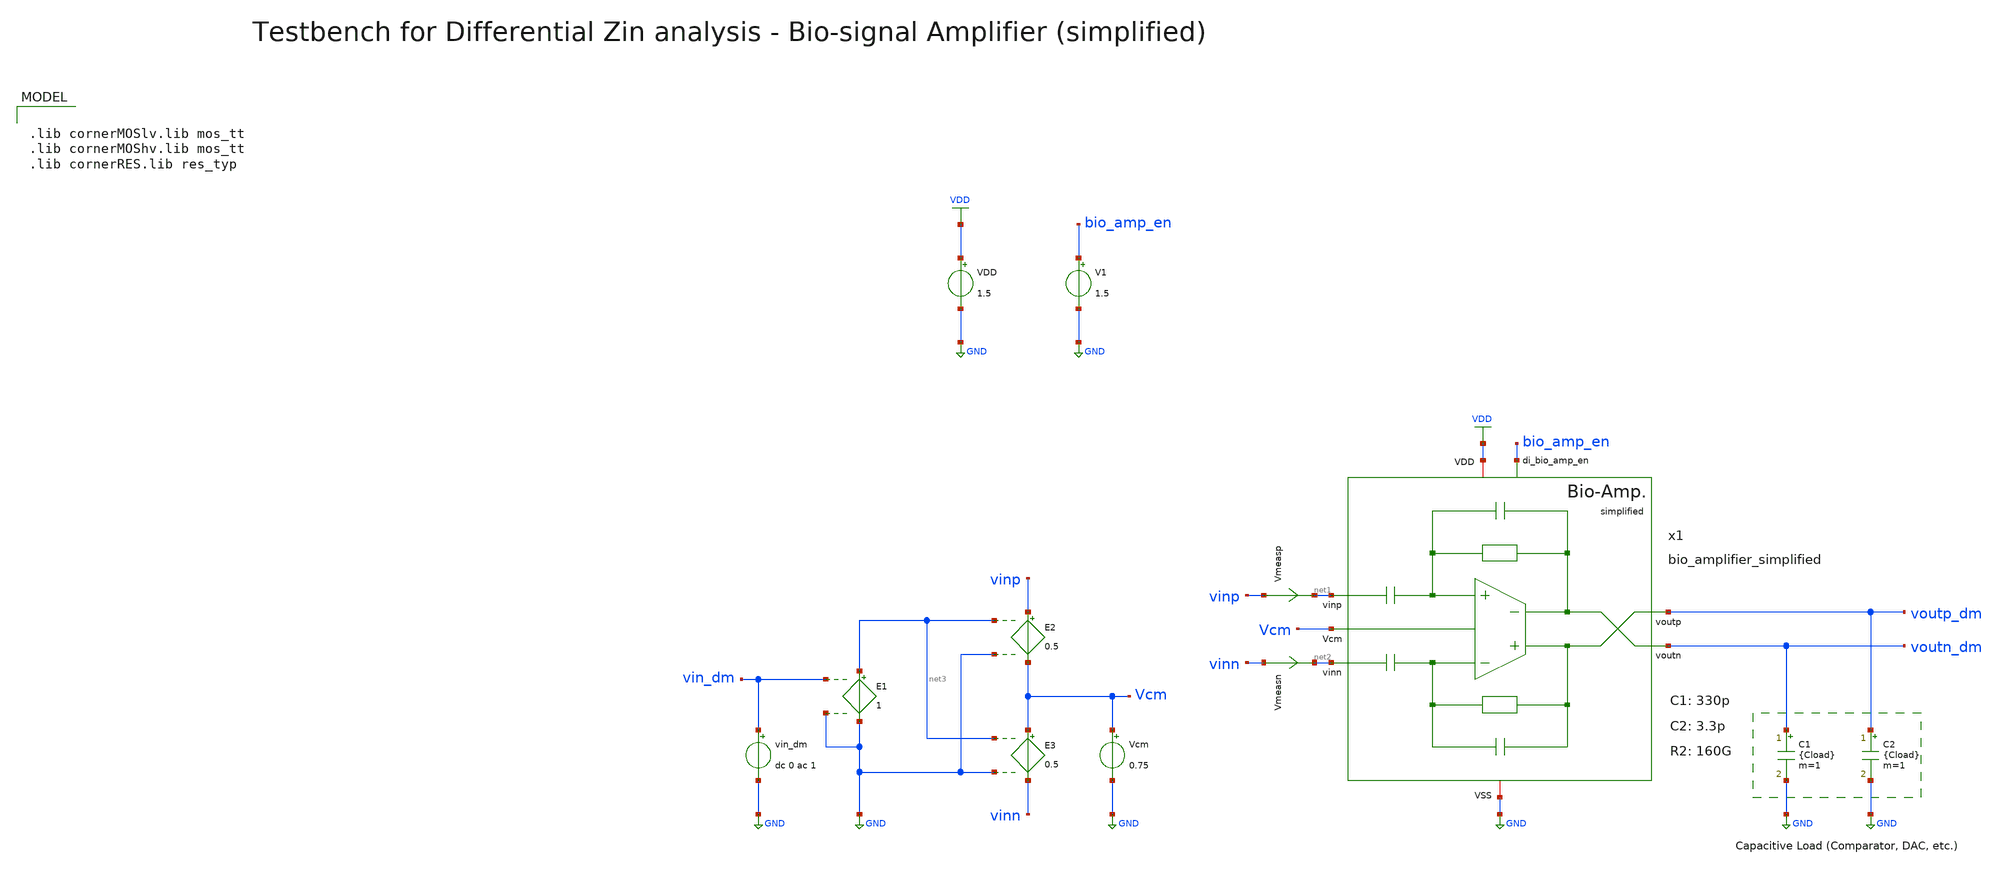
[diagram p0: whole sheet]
** sch_path: SG13G2_ATBS-ADC-main/xschem/bio_amplifier/testbenches/bio_amplifier_simplified_tb_Zin_dm.sch
**.subckt bio_amplifier_simplified_tb_Zin_dm
VDD VDD GND 1.5
C1 voutn_dm GND {Cload} m=1
C2 voutp_dm GND {Cload} m=1
V1 bio_amp_en GND 1.5
Vmeasp vinp net1 0
.save i(vmeasp)
Vmeasn vinn net2 0
.save i(vmeasn)
x1 voutp_dm bio_amp_en net1 Vcm voutn_dm net2 VDD GND bio_amplifier_simplified C1=330p C2=3.3p
+ R2=160G
Vcm Vcm GND 0.75
E3 Vcm vinn net3 GND 0.5
E2 vinp Vcm net3 GND 0.5
E1 net3 GND vin_dm GND 1
vin_dm vin_dm GND dc 0 ac 1
**** begin user architecture code


.param temp=27
* 227.56fF DAC
.param Cload=227.56f
.options savecurrents klu method=gear reltol=1e-2 abstol=1e-15 gmin=1e-15 rshunt=1e12
.control

optran 0 0 0 1u 1m 0

save all

set wr_vecnames
set wr_singlescale

* User Constants
let f_min = 10m
let f_max = 100
let fdc = 10

* Operating Point Analysis
op
remzerovec
write bio_amplifier_simplified_tb_Zin_dm.raw
set appendwrite

* AC Analysis
ac dec 101 $&const.f_min $&const.f_max
remzerovec
write bio_amplifier_simplified_tb_Zin_dm.raw

* Plotting Differential Mode Zin
* let Zin_dm = (v(vinp) - v(vinn)) / (i(Vmeasp) - i(Vmeasn))
* let Zin_dm = (v(vinp) - v(vinn)) / (i(Vmeasp) + i(Vmeasn))
let Zin_dm = (v(vinp) - v(vinn)) / i(Vmeasp)
* let Zin_dm = ((v(vinp) + v(vinn)) / 2) / i(Vmeasp)
plot Zin_dm ylabel 'DM Zin'

* Measurements
meas ac Zindc_dm find Zin_dm when frequency = 1
print Zindc_dm

meas ac Zindc_dm find Zin_dm when frequency = fdc
print Zindc_dm

* Write Data
set wr_vecnames
set wr_singlescale
wrdata
+ /foss/designs/SG13G2_ATBS-ADC-main/python/plot_simulations/data/bio_amplifier_simplified_tb_Zin_dm.txt v(Zin_dm)

*quit
.endc



.lib cornerMOSlv.lib mos_tt
.lib cornerMOShv.lib mos_tt
.lib cornerRES.lib res_typ

**** end user architecture code
**.ends
.GLOBAL GND
.GLOBAL VDD
.end
